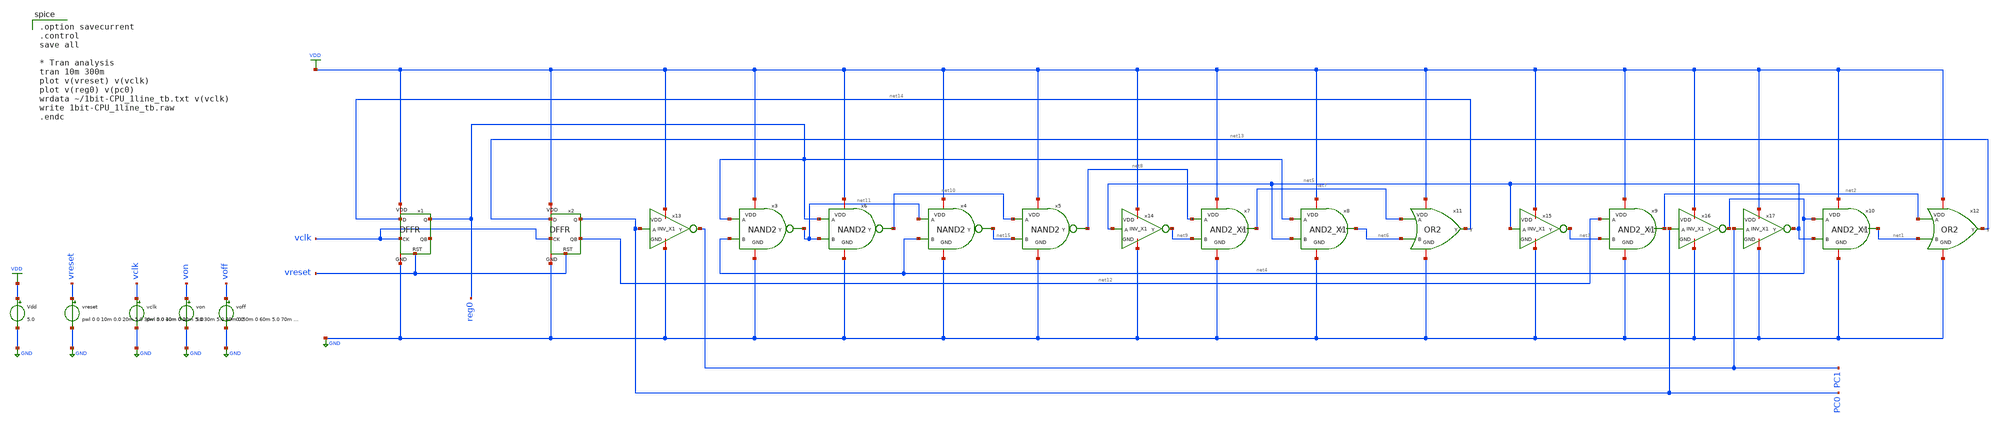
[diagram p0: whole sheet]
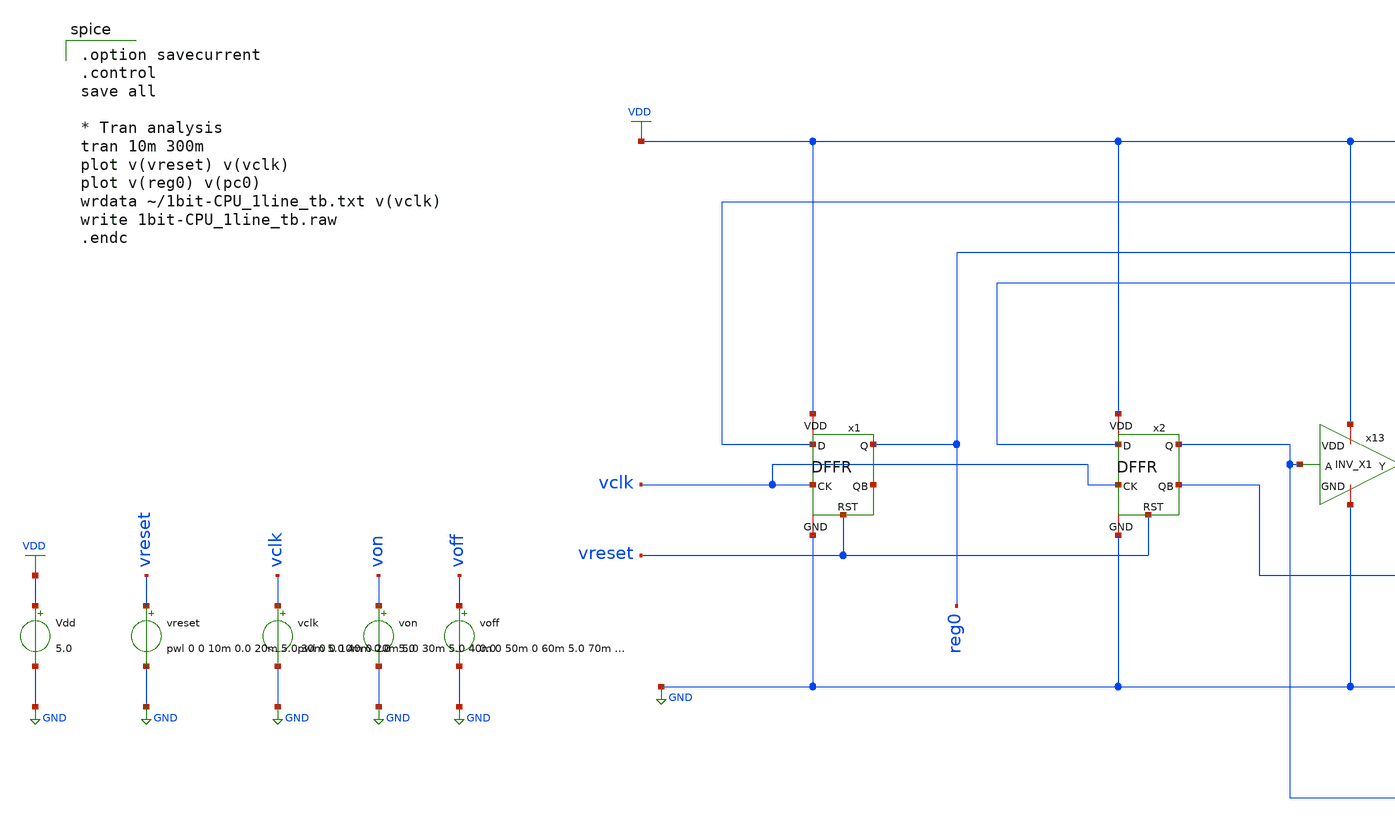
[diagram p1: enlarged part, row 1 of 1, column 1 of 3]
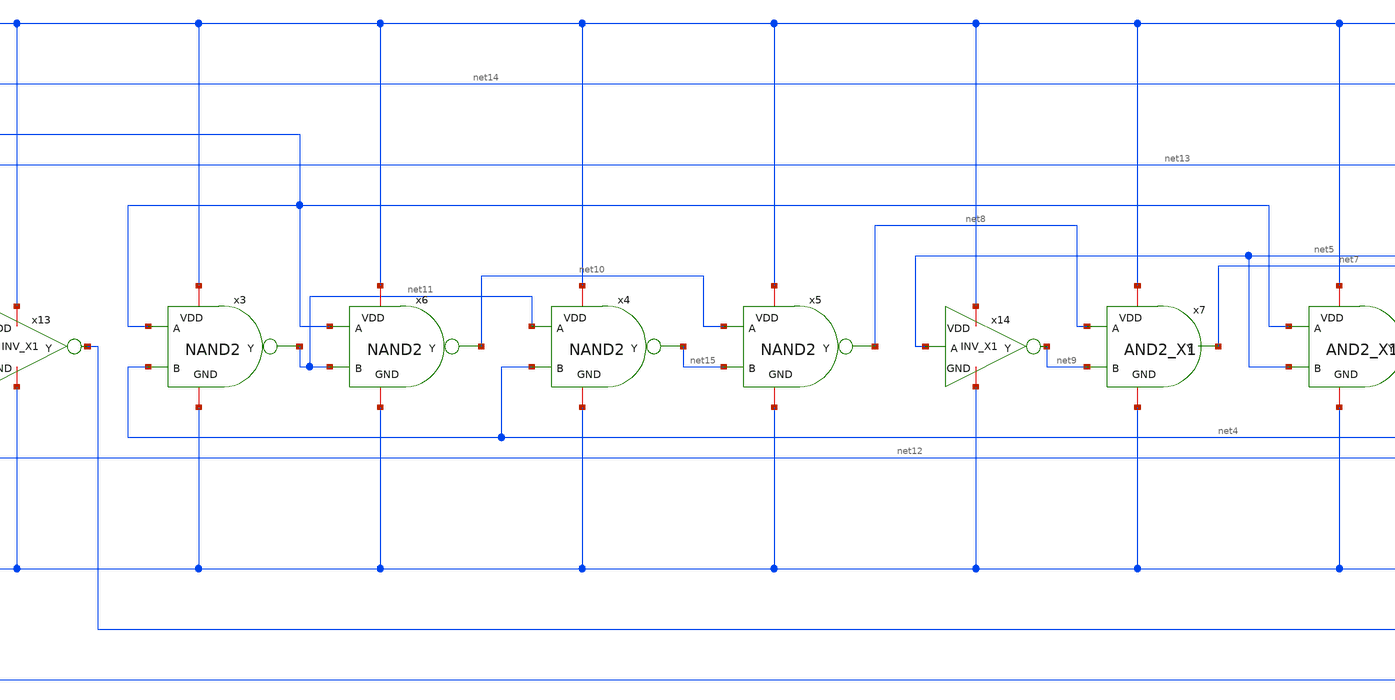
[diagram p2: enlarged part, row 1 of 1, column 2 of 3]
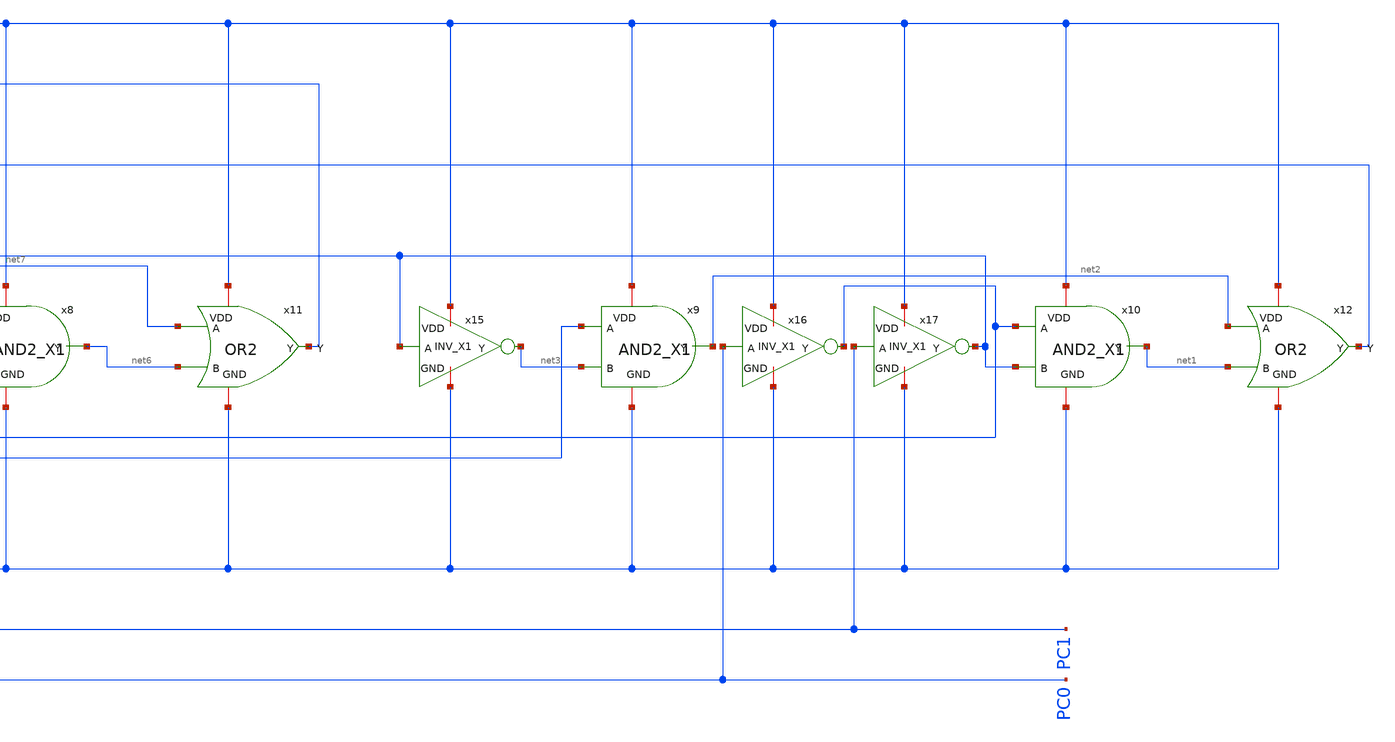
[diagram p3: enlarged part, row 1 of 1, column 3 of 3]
** sch_path: member_project/1bit-CPU_ALL/1bit-CPU_1line_tb.sch
**.subckt 1bit-CPU_1line_tb
x1 VDD net16 net14 reg0 vreset GND vclk DFFR
x2 VDD net12 net13 PC0 vreset GND vclk DFFR
x13 VDD PC0 PC1 GND INV_X1
x7 VDD net7 net8 net9 GND AND2_X1
x8 VDD net6 reg0 net5 GND AND2_X1
x9 VDD net2 net12 net3 GND AND2_X1
x10 VDD net1 net4 net5 GND AND2_X1
x11 VDD net14 net7 net6 GND OR2
x12 VDD net13 net2 net1 GND OR2
x14 VDD net5 net9 GND INV_X1
x15 VDD net5 net3 GND INV_X1
x16 VDD PC0 net4 GND INV_X1
x17 VDD PC1 net5 GND INV_X1
Vdd VDD GND 5.0
vreset vreset GND pwl 0 0 10m 0.0 20m 5.0 30m 5.0 40m 0.0
vclk vclk GND pwl 0 0 10m 0 20m 5.0 30m 5.0 40m 0 50m 0 60m 5.0 70m 5.0 80m 0 90m 0 100m 5.0 110m
+ 5.0 120m 0 130m 0 140m 5.0 150m 5.0 160m 0 170m 0 180m 5.0 190m 5.0 200m 0 210m 0 220m 5.0 230m 5.0
+ 240m 0 250m 0 260m 5.0 270m 5.0 280m 0 290m 0
x3 VDD net11 reg0 net4 GND NAND2
x4 VDD net15 net11 net4 GND NAND2
x5 VDD net8 net10 net15 GND NAND2
x6 VDD net10 reg0 net11 GND NAND2
von von GND 5.0
voff voff GND 0.0
**** begin user architecture code
 .include $::LIB/../ip62_models

.option savecurrent
.control
save all

* Tran analysis
tran 10m 300m
plot v(vreset) v(vclk)
plot v(reg0) v(pc0)
wrdata ~/1bit-CPU_1line_tb.txt v(vclk)
write 1bit-CPU_1line_tb.raw
.endc

**** end user architecture code
**.ends

* expanding   symbol:  IP62_5_stdcell/DFFR.sym # of pins=7
** sym_path: IP62_5_stdcell/DFFR.sym
** sch_path: IP62_5_stdcell/DFFR.sch
.subckt DFFR VDD QB D Q RST GND CK
*.iopin VDD
*.iopin GND
*.ipin CK
*.ipin D
*.opin Q
*.opin QB
*.ipin RST
XM2 net2 D VDD VDD PMOS w=10.2u l=1u as=0 ad=0 ps=0 pd=0 nrd=0 nrs=0 m=1
XM1 net3 CLK net2 VDD PMOS w=10.2u l=1u as=0 ad=0 ps=0 pd=0 nrd=0 nrs=0 m=1
XM11 net5 net8 VDD VDD PMOS w=10.2u l=1u as=0 ad=0 ps=0 pd=0 nrd=0 nrs=0 m=1
XM12 net3 CKB net5 VDD PMOS w=10.2u l=1u as=0 ad=0 ps=0 pd=0 nrd=0 nrs=0 m=1
XM15 net7 net3 VDD VDD PMOS w=10.2u l=1u as=0 ad=0 ps=0 pd=0 nrd=0 nrs=0 m=1
XM16 net8 RST net7 VDD PMOS w=10.2u l=1u as=0 ad=0 ps=0 pd=0 nrd=0 nrs=0 m=1
XM18 net9 net8 VDD VDD PMOS w=10.2u l=1u as=0 ad=0 ps=0 pd=0 nrd=0 nrs=0 m=1
XM19 net10 CKB net9 VDD PMOS w=10.2u l=1u as=0 ad=0 ps=0 pd=0 nrd=0 nrs=0 m=1
XM23 net12 net14 VDD VDD PMOS w=10.2u l=1u as=0 ad=0 ps=0 pd=0 nrd=0 nrs=0 m=1
XM24 net10 CLK net12 VDD PMOS w=10.2u l=1u as=0 ad=0 ps=0 pd=0 nrd=0 nrs=0 m=1
XM27 net15 net10 VDD VDD PMOS w=10.2u l=1u as=0 ad=0 ps=0 pd=0 nrd=0 nrs=0 m=1
XM28 net14 RST net15 VDD PMOS w=10.2u l=1u as=0 ad=0 ps=0 pd=0 nrd=0 nrs=0 m=1
XM31 QB net14 VDD VDD PMOS w=10.2u l=1u as=0 ad=0 ps=0 pd=0 nrd=0 nrs=0 m=1
XM33 Q QB VDD VDD PMOS w=10.2u l=1u as=0 ad=0 ps=0 pd=0 nrd=0 nrs=0 m=1
XM35 QB net14 GND GND NMOS w=3.4u l=1u as=0 ad=0 ps=0 pd=0 nrd=0 nrs=0 m=1
XM32 Q QB GND GND NMOS w=3.4u l=1u as=0 ad=0 ps=0 pd=0 nrd=0 nrs=0 m=1
XM29 net14 RST GND GND NMOS w=3.4u l=1u as=0 ad=0 ps=0 pd=0 nrd=0 nrs=0 m=1
XM30 net14 net10 GND GND NMOS w=3.4u l=1u as=0 ad=0 ps=0 pd=0 nrd=0 nrs=0 m=1
XM25 net10 CKB net13 GND NMOS w=3.4u l=1u as=0 ad=0 ps=0 pd=0 nrd=0 nrs=0 m=1
XM26 net13 net14 GND GND NMOS w=3.4u l=1u as=0 ad=0 ps=0 pd=0 nrd=0 nrs=0 m=1
XM20 net10 CLK net11 GND NMOS w=3.4u l=1u as=0 ad=0 ps=0 pd=0 nrd=0 nrs=0 m=1
XM21 net11 net8 GND GND NMOS w=3.4u l=1u as=0 ad=0 ps=0 pd=0 nrd=0 nrs=0 m=1
XM17 net8 net3 GND GND NMOS w=3.4u l=1u as=0 ad=0 ps=0 pd=0 nrd=0 nrs=0 m=1
XM22 net8 RST GND GND NMOS w=3.4u l=1u as=0 ad=0 ps=0 pd=0 nrd=0 nrs=0 m=1
XM13 net3 CLK net6 GND NMOS w=3.4u l=1u as=0 ad=0 ps=0 pd=0 nrd=0 nrs=0 m=1
XM14 net6 net8 GND GND NMOS w=3.4u l=1u as=0 ad=0 ps=0 pd=0 nrd=0 nrs=0 m=1
XM7 net3 CKB net4 GND NMOS w=3.4u l=1u as=0 ad=0 ps=0 pd=0 nrd=0 nrs=0 m=1
XM8 net4 D GND GND NMOS w=3.4u l=1u as=0 ad=0 ps=0 pd=0 nrd=0 nrs=0 m=1
XM3 net1 CK VDD VDD PMOS w=10.2u l=1u as=0 ad=0 ps=0 pd=0 nrd=0 nrs=0 m=1
XM4 CLK net1 VDD VDD PMOS w=10.2u l=1u as=0 ad=0 ps=0 pd=0 nrd=0 nrs=0 m=1
XM5 CKB CLK VDD VDD PMOS w=10.2u l=1u as=0 ad=0 ps=0 pd=0 nrd=0 nrs=0 m=1
XM34 net1 CK GND GND NMOS w=3.4u l=1u as=0 ad=0 ps=0 pd=0 nrd=0 nrs=0 m=1
XM6 CLK net1 GND GND NMOS w=3.4u l=1u as=0 ad=0 ps=0 pd=0 nrd=0 nrs=0 m=1
XM9 CKB CLK GND GND NMOS w=3.4u l=1u as=0 ad=0 ps=0 pd=0 nrd=0 nrs=0 m=1
.ends


* expanding   symbol:  IP62_5_stdcell/INV_X1.sym # of pins=4
** sym_path: IP62_5_stdcell/INV_X1.sym
** sch_path: IP62_5_stdcell/INV_X1.sch
.subckt INV_X1 VDD A Y GND
*.ipin A
*.opin Y
*.iopin GND
*.iopin VDD
XM7 Y A VDD VDD PMOS w=10.2u l=1u as=0 ad=0 ps=0 pd=0 nrd=0 nrs=0 m=1
XM2 Y A GND GND NMOS w=3.4u l=1u as=0 ad=0 ps=0 pd=0 nrd=0 nrs=0 m=1
.ends


* expanding   symbol:  IP62_5_stdcell/AND2_X1.sym # of pins=5
** sym_path: IP62_5_stdcell/AND2_X1.sym
** sch_path: IP62_5_stdcell/AND2_X1.sch
.subckt AND2_X1 VDD Y A B GND
*.opin Y
*.ipin A
*.ipin B
*.iopin VDD
*.iopin GND
XM7 net1 B VDD VDD PMOS w=10.2u l=1u as=0 ad=0 ps=0 pd=0 nrd=0 nrs=0 m=1
XM1 net1 A VDD VDD PMOS w=10.2u l=1u as=0 ad=0 ps=0 pd=0 nrd=0 nrs=0 m=1
XM2 Y net1 VDD VDD PMOS w=10.2u l=1u as=0 ad=0 ps=0 pd=0 nrd=0 nrs=0 m=1
XM3 Y net1 GND GND NMOS w=3.4u l=1u as=0 ad=0 ps=0 pd=0 nrd=0 nrs=0 m=1
XM4 net1 A net2 GND NMOS w=3.4u l=1u as=0 ad=0 ps=0 pd=0 nrd=0 nrs=0 m=1
XM5 net2 B GND GND NMOS w=3.4u l=1u as=0 ad=0 ps=0 pd=0 nrd=0 nrs=0 m=1
.ends


* expanding   symbol:  IP62_5_stdcell/OR2.sym # of pins=5
** sym_path: IP62_5_stdcell/OR2.sym
** sch_path: IP62_5_stdcell/OR2.sch
.subckt OR2 VDD Y A B GND
*.ipin A
*.ipin B
*.opin Y
*.iopin VDD
*.iopin GND
XM7 net2 B VDD VDD PMOS w=10.2u l=1u as=0 ad=0 ps=0 pd=0 nrd=0 nrs=0 m=1
XM2 net1 A net2 VDD PMOS w=10.2u l=1u as=0 ad=0 ps=0 pd=0 nrd=0 nrs=0 m=1
XM4 Y net1 VDD VDD PMOS w=10.2u l=1u as=0 ad=0 ps=0 pd=0 nrd=0 nrs=0 m=1
XM1 net1 B GND GND NMOS w=3.4u l=1u as=0 ad=0 ps=0 pd=0 nrd=0 nrs=0 m=1
XM3 net1 A GND GND NMOS w=3.4u l=1u as=0 ad=0 ps=0 pd=0 nrd=0 nrs=0 m=1
XM5 Y net1 GND GND NMOS w=3.4u l=1u as=0 ad=0 ps=0 pd=0 nrd=0 nrs=0 m=1
.ends


* expanding   symbol:  IP62_5_stdcell/NAND2.sym # of pins=5
** sym_path: IP62_5_stdcell/NAND2.sym
** sch_path: IP62_5_stdcell/NAND2.sch
.subckt NAND2 VDD Y A B GND
*.ipin B
*.ipin A
*.opin Y
*.iopin GND
*.iopin VDD
XM7 Y A VDD VDD PMOS w=10.2u l=1u as=0 ad=0 ps=0 pd=0 nrd=0 nrs=0 m=1
XM1 Y B VDD VDD PMOS w=10.2u l=1u as=0 ad=0 ps=0 pd=0 nrd=0 nrs=0 m=1
XM2 Y B net1 GND NMOS w=3.4u l=1u as=0 ad=0 ps=0 pd=0 nrd=0 nrs=0 m=1
XM3 net1 A GND GND NMOS w=3.4u l=1u as=0 ad=0 ps=0 pd=0 nrd=0 nrs=0 m=1
.ends

.GLOBAL VDD
.GLOBAL GND
.end
